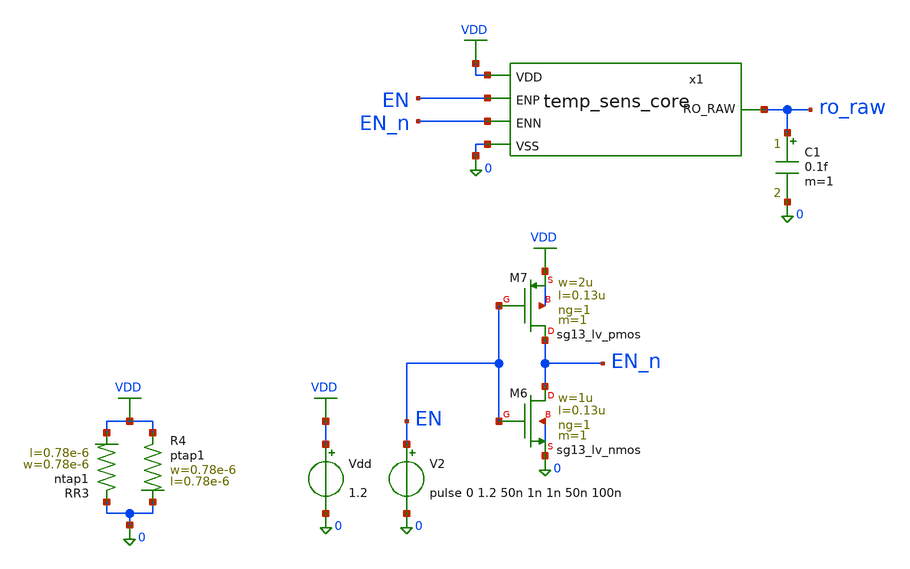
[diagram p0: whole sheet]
** sch_path: TSENSE8490-main/schematic/xschem/analog/temp-sens-core/testbenches/temp-sens-core_en-pv-tb.sch
**.subckt temp-sens-core_en-pv-tb
Vdd VDD 0 1.2
XR3 0 VDD ntap1 R=262.8 w=0.78e-6 l=0.78e-6
XR4 VDD 0 ptap1 R=262.8 w=0.78e-6 l=0.78e-6
XM6 EN_n EN 0 0 sg13_lv_nmos w=1u l=0.13u ng=1 m=1 mm_ok=1
XM7 EN_n EN VDD VDD sg13_lv_pmos w=2u l=0.13u ng=1 m=1 mm_ok=1
V2 EN 0 pulse 0 1.2 50n 1n 1n 50n 100n
x1 EN EN_n ro_raw VDD 0 temp_sens_core
C1 ro_raw 0 0.1f m=1
**** begin user architecture code



** ngr_lib cornerMOSlv.lib mos_tt mos_ff mos_ss mos_sf mos_fs mos_tt_mismatch
** ngr_lib cornerRES.lib res_typ res_typ_mismatch res_wcs_mismatch
** ngr_out f

.lib cornerMOSlv.lib mos_tt
.lib cornerRES.lib res_typ

.option rshunt=1e12
.option klu
.control

tran 0.1n 1u

meas tran tperiod   TRIG v(ro_raw) VAL=0.9 RISE=2 TD=60n   TARG v(ro_raw) VAL=0.9 RISE=3 TD=60n

let f = 1/tperiod
print f

** write temp-sens-core_pvt_tt.raw time ro_raw en en_n f
write $rawfile time ro_raw en en_n f

.endc






.include sg13cmos5l_stdcell.spice



**** end user architecture code
**.ends

* expanding   symbol:  analog/temp-sens-core/temp_sens_core.sym # of pins=5
** sym_path: TSENSE8490-main/schematic/xschem/lvs-view/analog/temp-sens-core/temp_sens_core.sym
** sch_path: TSENSE8490-main/schematic/xschem/lvs-view/analog/temp-sens-core/temp_sens_core.sch
.subckt temp_sens_core ENP ENN RO_RAW VDD VSS
*.opin RO_RAW
*.iopin VDD
*.iopin VSS
*.ipin ENP
*.ipin ENN
XM1 net11 vgp VDD VDD sg13_lv_pmos w=1.5u l={lstarv} ng=1 m=1 mm_ok=1
XM21 vgp ENP VDD VDD sg13_lv_pmos w=10u l=0.13u ng=1 m=1 mm_ok=1
XM22 vgn ENN VSS VSS sg13_lv_nmos w=10u l=0.13u ng=1 m=1 mm_ok=1
XM23 vgp vgp VDD VDD sg13_lv_pmos w=1.5u l={lstarv} ng=1 m=1 mm_ok=1
XM24 vgn vgn VSS VSS sg13_lv_nmos w=1.5u l={lstarv} ng=1 m=1 mm_ok=1
XM4 net20 vgn VSS VSS sg13_lv_nmos w=1.5u l={lstarv} ng=1 m=1 mm_ok=1
XM5 net12 vgp VDD VDD sg13_lv_pmos w=1.5u l={lstarv} ng=1 m=1 mm_ok=1
XM8 net21 vgn VSS VSS sg13_lv_nmos w=1.5u l={lstarv} ng=1 m=1 mm_ok=1
XM9 net13 vgp VDD VDD sg13_lv_pmos w=1.5u l={lstarv} ng=1 m=1 mm_ok=1
XM12 net22 vgn VSS VSS sg13_lv_nmos w=1.5u l={lstarv} ng=1 m=1 mm_ok=1
XM13 net14 vgp VDD VDD sg13_lv_pmos w=1.5u l={lstarv} ng=1 m=1 mm_ok=1
XM16 net23 vgn VSS VSS sg13_lv_nmos w=1.5u l={lstarv} ng=1 m=1 mm_ok=1
XM17 net15 vgp VDD VDD sg13_lv_pmos w=1.5u l={lstarv} ng=1 m=1 mm_ok=1
XM20 net24 vgn VSS VSS sg13_lv_nmos w=1.5u l={lstarv} ng=1 m=1 mm_ok=1
XM25 net16 vgp VDD VDD sg13_lv_pmos w=1.5u l={lstarv} ng=1 m=1 mm_ok=1
XM28 net25 vgn VSS VSS sg13_lv_nmos w=1.5u l={lstarv} ng=1 m=1 mm_ok=1
XM29 net17 vgp VDD VDD sg13_lv_pmos w=1.5u l={lstarv} ng=1 m=1 mm_ok=1
XM32 net26 vgn VSS VSS sg13_lv_nmos w=1.5u l={lstarv} ng=1 m=1 mm_ok=1
XM2 VSS net1 vgp VDD sg13_lv_pmos w=1u l=0.13u ng=1 m=1 mm_ok=1
XM3 VDD net2 vgn VSS sg13_lv_nmos w=1u l=0.13u ng=1 m=1 mm_ok=1
XR6 VDD net1 sub! rsil w=0.5e-6 l=75e-6 m=1 mm_ok=1
XR7 net1 VSS sub! rsil w=0.5e-6 l=10e-6 m=1 mm_ok=1
XR1 net2 VSS sub! rsil w=0.5e-6 l=75e-6 m=1 mm_ok=1
XR2 VDD net2 sub! rsil w=0.5e-6 l=10e-6 m=1 mm_ok=1
XM6 net18 vgp VDD VDD sg13_lv_pmos w=1.5u l={lstarv} ng=1 m=1 mm_ok=1
XM7 net27 vgn VSS VSS sg13_lv_nmos w=1.5u l={lstarv} ng=1 m=1 mm_ok=1
XM10 net19 vgp VDD VDD sg13_lv_pmos w=1.5u l={lstarv} ng=1 m=1 mm_ok=1
XM11 net28 vgn VSS VSS sg13_lv_nmos w=1.5u l={lstarv} ng=1 m=1 mm_ok=1
XM14 RO_RAW ENP VDD VDD sg13_lv_pmos w=0.3u l=0.13u ng=1 m=1 mm_ok=1
XM15 net3 RO_RAW net20 VSS sg13_lv_nmos w=0.74u l=0.13u ng=1 m=1 mm_ok=1
XM18 net11 RO_RAW net3 VDD sg13_lv_pmos w=1.12u l=0.13u ng=1 m=1 mm_ok=1
XM19 net4 net3 net21 VSS sg13_lv_nmos w=0.74u l=0.13u ng=1 m=1 mm_ok=1
XM26 net12 net3 net4 VDD sg13_lv_pmos w=1.12u l=0.13u ng=1 m=1 mm_ok=1
XM27 net5 net4 net22 VSS sg13_lv_nmos w=0.74u l=0.13u ng=1 m=1 mm_ok=1
XM30 net13 net4 net5 VDD sg13_lv_pmos w=1.12u l=0.13u ng=1 m=1 mm_ok=1
XM31 net6 net5 net23 VSS sg13_lv_nmos w=0.74u l=0.13u ng=1 m=1 mm_ok=1
XM33 net14 net5 net6 VDD sg13_lv_pmos w=1.12u l=0.13u ng=1 m=1 mm_ok=1
XM34 net7 net6 net24 VSS sg13_lv_nmos w=0.74u l=0.13u ng=1 m=1 mm_ok=1
XM35 net15 net6 net7 VDD sg13_lv_pmos w=1.12u l=0.13u ng=1 m=1 mm_ok=1
XM36 net8 net7 net25 VSS sg13_lv_nmos w=0.74u l=0.13u ng=1 m=1 mm_ok=1
XM37 net16 net7 net8 VDD sg13_lv_pmos w=1.12u l=0.13u ng=1 m=1 mm_ok=1
XM38 net9 net8 net26 VSS sg13_lv_nmos w=0.74u l=0.13u ng=1 m=1 mm_ok=1
XM39 net17 net8 net9 VDD sg13_lv_pmos w=1.12u l=0.13u ng=1 m=1 mm_ok=1
XM40 net10 net9 net27 VSS sg13_lv_nmos w=0.74u l=0.13u ng=1 m=1 mm_ok=1
XM41 net18 net9 net10 VDD sg13_lv_pmos w=1.12u l=0.13u ng=1 m=1 mm_ok=1
XM42 RO_RAW net10 net28 VSS sg13_lv_nmos w=0.74u l=0.13u ng=1 m=1 mm_ok=1
XM43 net19 net10 RO_RAW VDD sg13_lv_pmos w=1.12u l=0.13u ng=1 m=1 mm_ok=1
.ends

.GLOBAL VDD
.end
